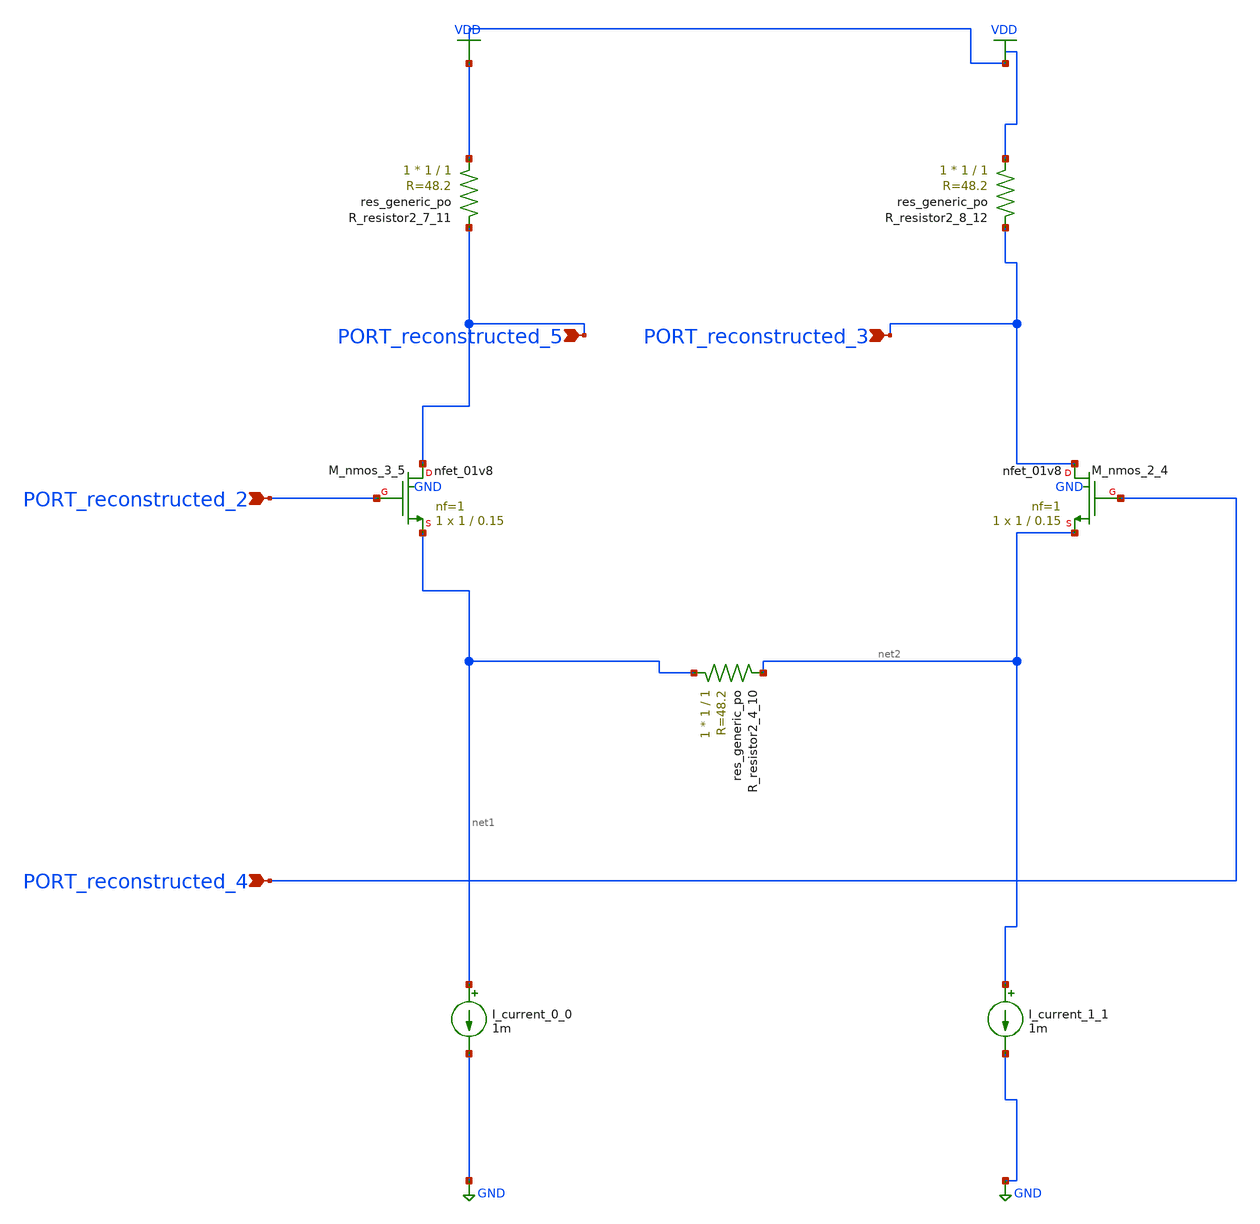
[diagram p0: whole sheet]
** sch_path: schematics/AMSNet/806.sch
**.subckt 806 PORT_reconstructed_3 PORT_reconstructed_4 PORT_reconstructed_2 PORT_reconstructed_5
*.ipin PORT_reconstructed_3
*.ipin PORT_reconstructed_4
*.ipin PORT_reconstructed_2
*.ipin PORT_reconstructed_5
I_current_0_0 net1 GND 1m
I_current_1_1 net2 GND 1m
XM_nmos_2_4 PORT_reconstructed_3 PORT_reconstructed_4 net2 GND sky130_fd_pr__nfet_01v8 L=0.15 W=1 nf=1
+ ad='int((1 + 1)/2) * 1 / 1 * 0.29' as='int((1 + 2)/2) * 1 / 1 * 0.29' pd='2*int((1 + 1)/2) * (1 / 1 + 0.29)'
+ ps='2*int((1 + 2)/2) * (1 / 1 + 0.29)' nrd='0.29 / 1 ' nrs='0.29 / 1 ' sa=0 sb=0 sd=0 mult=1 m=1
XM_nmos_3_5 PORT_reconstructed_5 PORT_reconstructed_2 net1 GND sky130_fd_pr__nfet_01v8 L=0.15 W=1 nf=1
+ ad='int((1 + 1)/2) * 1 / 1 * 0.29' as='int((1 + 2)/2) * 1 / 1 * 0.29' pd='2*int((1 + 1)/2) * (1 / 1 + 0.29)'
+ ps='2*int((1 + 2)/2) * (1 / 1 + 0.29)' nrd='0.29 / 1 ' nrs='0.29 / 1 ' sa=0 sb=0 sd=0 mult=1 m=1
XR_resistor2_4_10 net1 net2 sky130_fd_pr__res_generic_po W=1 L=1 m=1
XR_resistor2_7_11 VDD PORT_reconstructed_5 sky130_fd_pr__res_generic_po W=1 L=1 m=1
XR_resistor2_8_12 VDD PORT_reconstructed_3 sky130_fd_pr__res_generic_po W=1 L=1 m=1
**.ends
.GLOBAL GND
.GLOBAL VDD
.end
